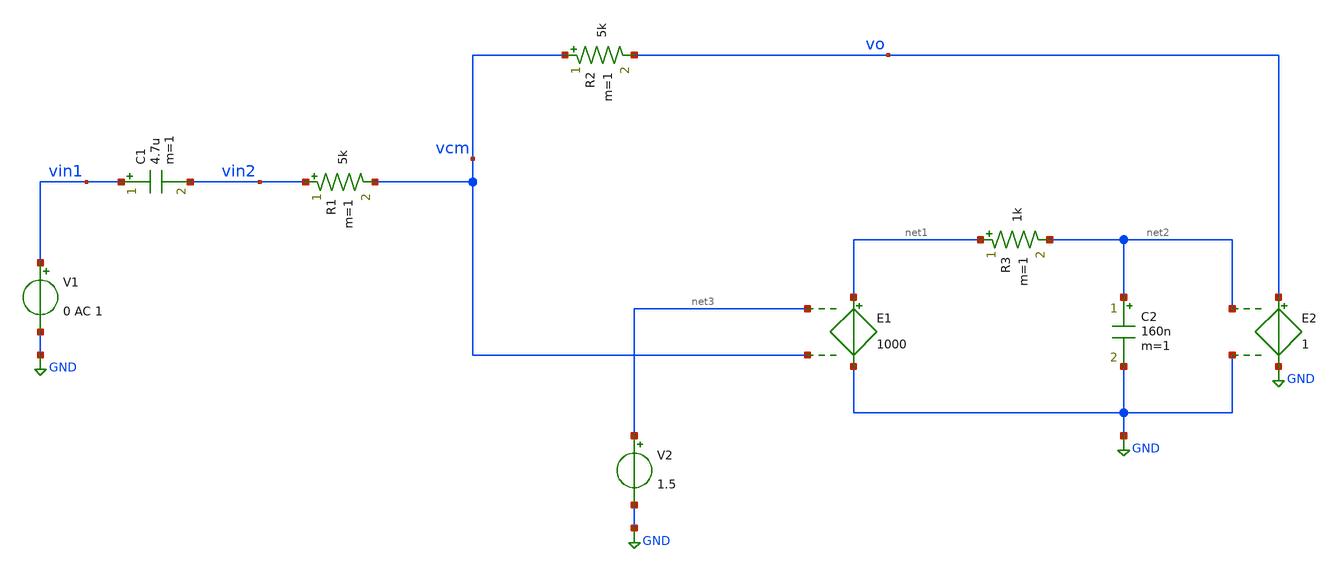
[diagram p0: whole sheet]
** sch_path: xschem/xschem/bandpass.sch
**.subckt bandpass
V1 vin1 GND 0 AC 1
C1 vin1 vin2 4.7u m=1
R1 vin2 vcm 5k m=1
V2 net3 GND 1.5
R2 vcm vo 5k m=1
E1 net1 GND net3 vcm 1000
E2 vo GND net2 GND 1
R3 net1 net2 1k m=1
C2 net2 GND 160n m=1
**** begin user architecture code



.control
OP
save all
write mic.raw
set appendwrite
AC DEC 100 1 10e6
write mic.raw
**
 meas ac gain_db MAX vdb(vo) FROM=0.1 TO=10e6
  LET f3db = gain_db - 3.0
  print f3db
  plot vdb(vo)
  MEAS AC fzero WHEN vdb(vo)=f3db RISE=1
  MEAS AC fpole WHEN vdb(vo)=f3db FALL=1
**  MEAS AC fmid WHEN vdb(vo)=gain_db
**Phase Measurement
  LET phase_deg = cph(vo)*180/PI
  MEAS AC phase_zero FIND phase_deg AT=fzero
  MEAS AC phase_pole FIND phase_deg AT=fpole
**  MEAS AC phase_mid FIND phase_deg AT=fmid
**MEAS fzero fpole using
  LET phase_zero_ph = phase_mid-45
  **MEAS AC fzero_ph WHEN phase_deg=phase_zero_ph
  **tran 1u 5m
.endc
.end



**** end user architecture code
**.ends
.GLOBAL GND
.end
